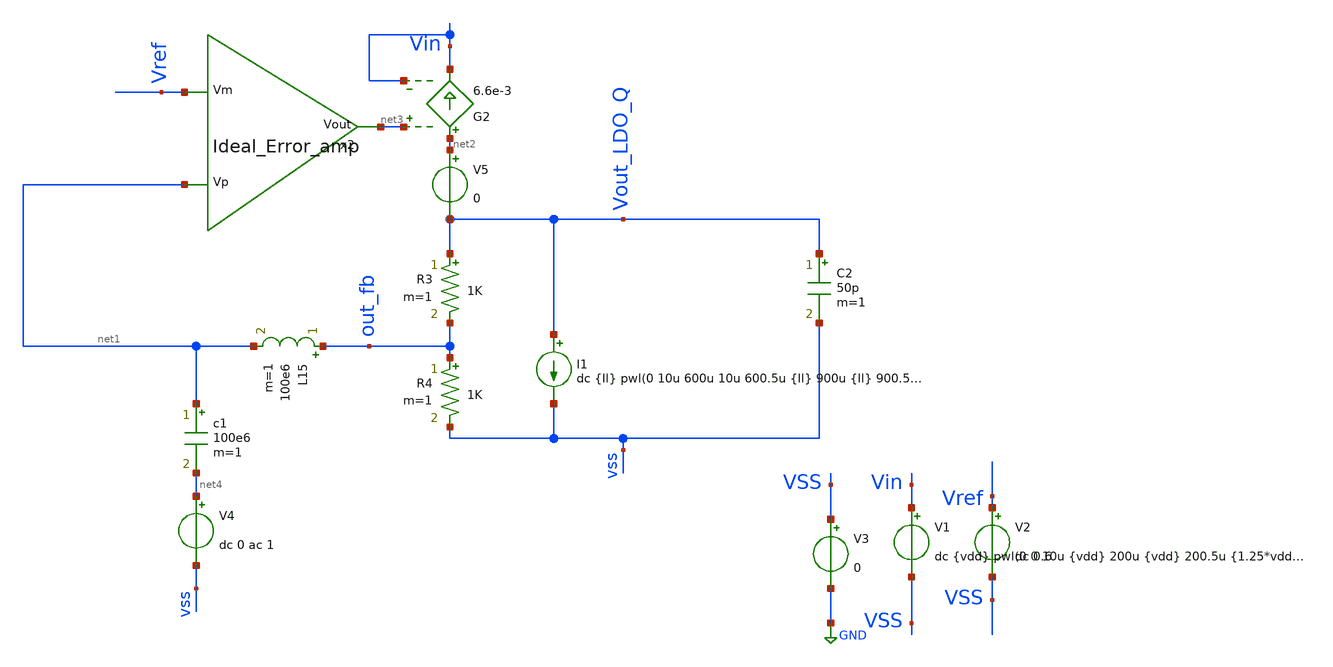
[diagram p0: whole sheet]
** sch_path: EE_628_LDO/LDO_STB_large_LC.sch
* Copyright 2023 IHP PDK Authors
**.subckt LDO_STB_large_LC
L15 out_fb net1 100e6 m=1
c1 net1 net4 100e6 m=1
I1 Vout_LDO_Q vss dc {Il} pwl(0 10u 600u 10u 600.5u {Il} 900u {Il} 900.5u 10u)
C2 Vout_LDO_Q vss 50p m=1
G2 net2 Vin net3 Vin 6.6e-3
V5 net2 Vout_LDO_Q 0
x2 net3 Vref net1 Ideal_Error_amp
R3 Vout_LDO_Q out_fb 1K m=1
R4 out_fb vss 1K m=1
V2 Vref VSS dc 0.6
V3 VSS GND 0
V1 Vin VSS dc {vdd} pwl(0 0 10u {vdd} 200u {vdd} 200.5u {1.25*vdd} 500u {1.25*vdd} 500.5u {vdd})
V4 net4 vss dc 0 ac 1
**** begin user architecture code

* Control
.param B=0 temp=27 vdd=1.8 Il=2m Res=1Meg Cap=10p Gm=20m
.model mysw SW vt={vdd/2} ron=10k roff=10gig reltol=1e-4
.control
save all
ac dec 20 10 1e9
let phase=180/3.14*cph(out_fb)
plot vdb(out_fb)
plot phase
plot vdb(out_fb) phase xlog

let phase=180 + 180/3.14*cph(out_fb)
meas ac ugbw when vdb(out_fb)=0
meas ac pm find phase when vdb(out_fb)=0
meas ac gain find vdb(out_fb) at=10
*echo "ugbw,pm,gain" > ac.txt
*echo "mb1,$&ugbw,$&pm,$&gain" >> ac.txt
.endc


 * Model Corners
.lib /foss/pdks/sg13g2/libs.tech/ngspice/models/cornerMOSlv.lib mos_tt
.lib /foss/pdks/sg13g2/libs.tech/ngspice/models/cornerRES.lib res_typ
**.include $::CORNERS/ngspice/tt.spice
*.include $::CORNERS/ngspice/ff.spice
*.include $::CORNERS/ngspice/ss.spice
*.include $::CORNERS/ngspice/sf.spice
*.include $::CORNERS/ngspice/fs.spice

**** end user architecture code
**.ends

* expanding   symbol:  /foss/designs/EE628_LDO/Ideal_Error_amp.sym # of pins=3
** sym_path: EE_628_LDO/Ideal_Error_amp.sym
** sch_path: EE_628_LDO/Ideal_Error_amp.sch
.subckt Ideal_Error_amp Vout Vm Vp
*.ipin Vm
*.ipin Vp
*.opin Vout
E1 Vout GND net1 GND 1
**** begin user architecture code

.lib /foss/pdks/sg13g2/libs.tech/ngspice/models/cornerMOSlv.lib mos_tt
.lib /foss/pdks/sg13g2/libs.tech/ngspice/models/cornerRES.lib res_typ
**.lib /foss/pdks/sg13g2/libs.tech/ngspice/models/sg13g2_moslv_mod.lib mos_tt
**.lib /foss/pdks/sg13g2/libs.tech/ngspice/models/sg13g2_moslv_parm.lib mos_tt
**.lib /foss/pdks/sg13g2/libs.tech/ngspice/models/sg13g2_moslv_stat.lib mos_tt

**** end user architecture code
G1 GND net1 Vp Vm Gm
R1 net1 GND Res m=1
C1 net1 GND Cap m=1
V2 net2 GND dc 0.7 ac 1
V1 net3 GND dc 0.7
.ends

.GLOBAL GND
.end
